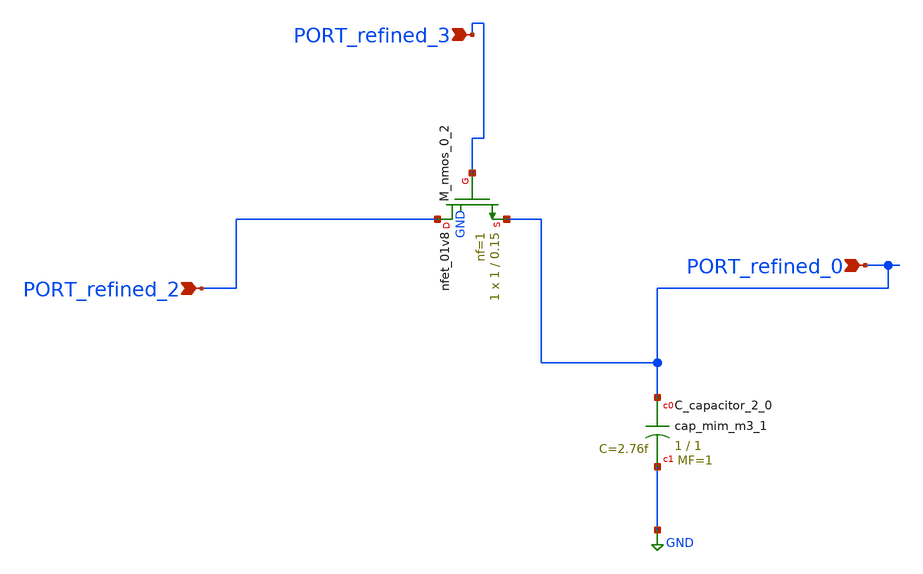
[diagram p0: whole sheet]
** sch_path: schematics/AMSNet/773.sch
**.subckt 773 PORT_refined_2 PORT_refined_0 PORT_refined_3
*.ipin PORT_refined_2
*.ipin PORT_refined_0
*.ipin PORT_refined_3
XC_capacitor_2_0 PORT_refined_0 GND sky130_fd_pr__cap_mim_m3_1 W=1 L=1 MF=1 m=1
XM_nmos_0_2 PORT_refined_2 PORT_refined_3 PORT_refined_0 GND sky130_fd_pr__nfet_01v8 L=0.15 W=1 nf=1
+ ad='int((1 + 1)/2) * 1 / 1 * 0.29' as='int((1 + 2)/2) * 1 / 1 * 0.29' pd='2*int((1 + 1)/2) * (1 / 1 + 0.29)'
+ ps='2*int((1 + 2)/2) * (1 / 1 + 0.29)' nrd='0.29 / 1 ' nrs='0.29 / 1 ' sa=0 sb=0 sd=0 mult=1 m=1
**.ends
.GLOBAL GND
.end
